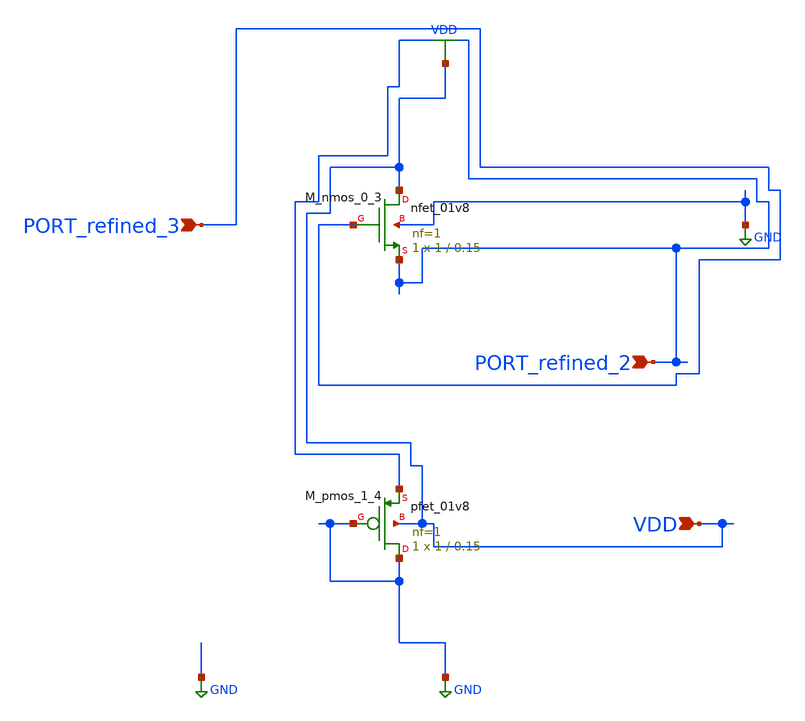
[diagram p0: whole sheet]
** sch_path: schematics/AMSNet/105.sch
**.subckt 105 PORT_refined_3 PORT_refined_2 VDD
*.ipin PORT_refined_3
*.ipin PORT_refined_2
*.ipin VDD
XM_nmos_0_3 VDD PORT_refined_3 PORT_refined_2 GND sky130_fd_pr__nfet_01v8 L=0.15 W=1 nf=1 ad='int((1 + 1)/2) * 1 / 1 * 0.29'
+ as='int((1 + 2)/2) * 1 / 1 * 0.29' pd='2*int((1 + 1)/2) * (1 / 1 + 0.29)' ps='2*int((1 + 2)/2) * (1 / 1 + 0.29)'
+ nrd='0.29 / 1 ' nrs='0.29 / 1 ' sa=0 sb=0 sd=0 mult=1 m=1
XM_pmos_1_4 GND GND PORT_refined_2 VDD sky130_fd_pr__pfet_01v8 L=0.15 W=1 nf=1 ad='int((1 + 1)/2) * 1 / 1 * 0.29'
+ as='int((1 + 2)/2) * 1 / 1 * 0.29' pd='2*int((1 + 1)/2) * (1 / 1 + 0.29)' ps='2*int((1 + 2)/2) * (1 / 1 + 0.29)'
+ nrd='0.29 / 1 ' nrs='0.29 / 1 ' sa=0 sb=0 sd=0 mult=1 m=1
**.ends
.GLOBAL GND
.GLOBAL VDD
.end
